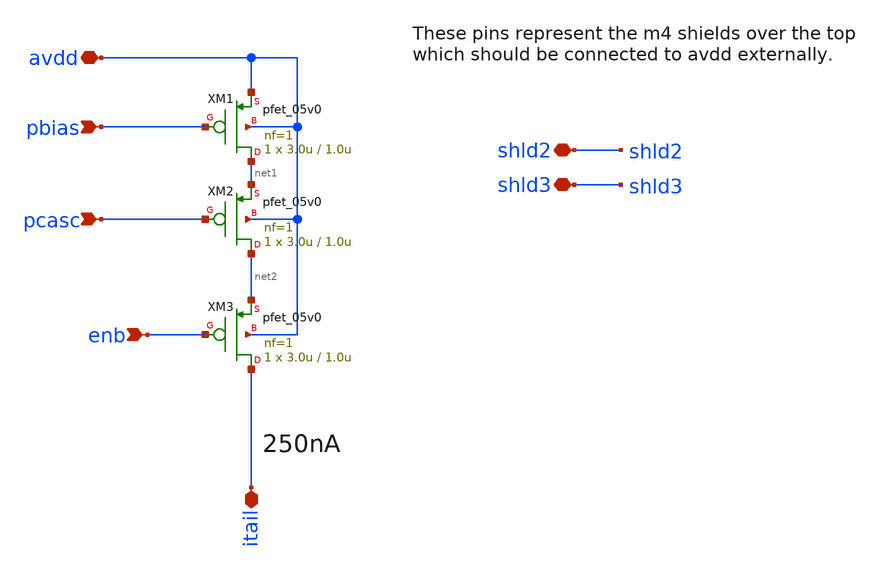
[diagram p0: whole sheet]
** sch_path: projects/programmable_transceiver_platform/analog/core_support/biasgen/xschem/bias_pstack.sch
**.subckt bias_pstack avdd itail enb pcasc pbias shld2 shld3
*.iopin avdd
*.iopin itail
*.ipin enb
*.ipin pcasc
*.ipin pbias
*.iopin shld2
*.iopin shld3
XM1 net1 pbias avdd avdd pfet_05v0 L=1.0u W=3.0u nf=1 ad='int((nf+1)/2) * W/nf * 0.18u' as='int((nf+2)/2) * W/nf * 0.18u'
+ pd='2*int((nf+1)/2) * (W/nf + 0.18u)' ps='2*int((nf+2)/2) * (W/nf + 0.18u)' nrd='0.18u / W' nrs='0.18u / W'
+ sa=0 sb=0 sd=0 m=1 par=1
XM2 net2 pcasc net1 avdd pfet_05v0 L=1.0u W=3.0u nf=1 ad='int((nf+1)/2) * W/nf * 0.18u' as='int((nf+2)/2) * W/nf * 0.18u'
+ pd='2*int((nf+1)/2) * (W/nf + 0.18u)' ps='2*int((nf+2)/2) * (W/nf + 0.18u)' nrd='0.18u / W' nrs='0.18u / W'
+ sa=0 sb=0 sd=0 m=1 par=1
XM3 itail enb net2 avdd pfet_05v0 L=1.0u W=3.0u nf=1 ad='int((nf+1)/2) * W/nf * 0.18u' as='int((nf+2)/2) * W/nf * 0.18u'
+ pd='2*int((nf+1)/2) * (W/nf + 0.18u)' ps='2*int((nf+2)/2) * (W/nf + 0.18u)' nrd='0.18u / W' nrs='0.18u / W'
+ sa=0 sb=0 sd=0 m=1 par=1
**.ends
.end
